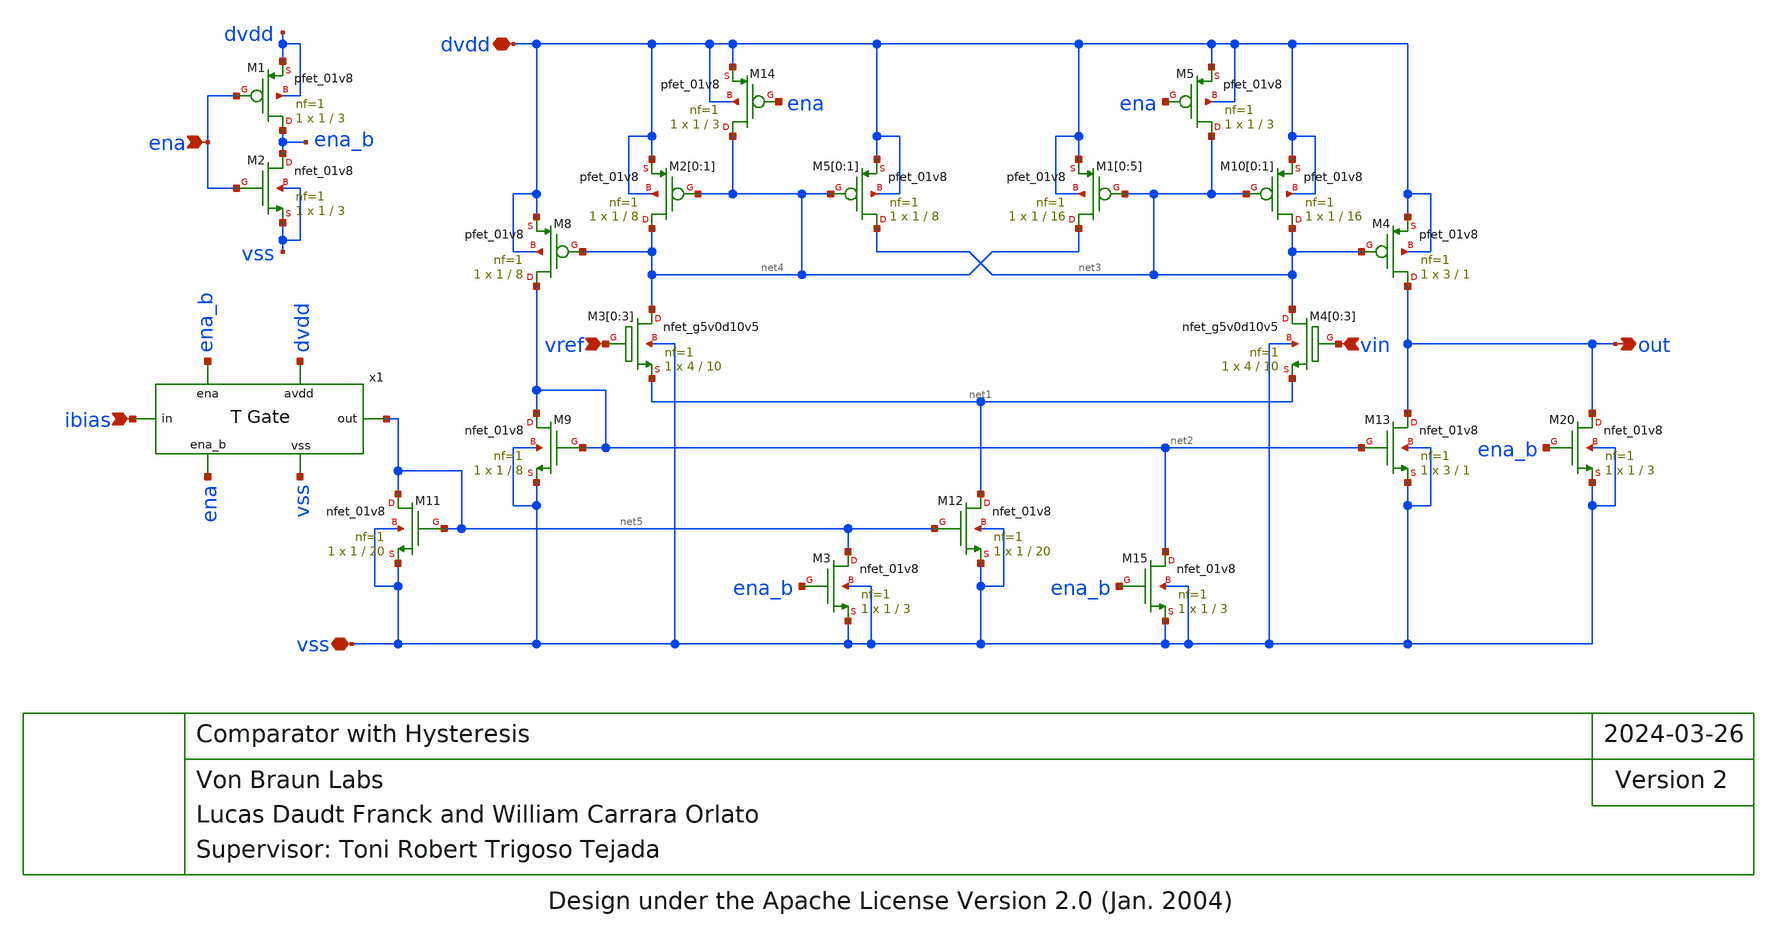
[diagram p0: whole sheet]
** sch_path: blocks/comp_hyst/xschem/comp_hyst.sch
* Design under the Apache License Version 2.0 (Jan. 2004)
**.subckt comp_hyst dvdd vref vin out ibias ena vss
*.iopin dvdd
*.ipin vref
*.ipin vin
*.opin out
*.ipin ibias
*.ipin ena
*.iopin vss
XM5[0] net3 net4 dvdd dvdd sky130_fd_pr__pfet_01v8 L=8 W=1 nf=1 ad='int((nf+1)/2) * W/nf * 0.29' as='int((nf+2)/2) * W/nf * 0.29'
+ pd='2*int((nf+1)/2) * (W/nf + 0.29)' ps='2*int((nf+2)/2) * (W/nf + 0.29)' nrd='0.29 / W' nrs='0.29 / W'
+ sa=0 sb=0 sd=0 mult=1 m=1
XM5[1] net3 net4 dvdd dvdd sky130_fd_pr__pfet_01v8 L=8 W=1 nf=1 ad='int((nf+1)/2) * W/nf * 0.29' as='int((nf+2)/2) * W/nf * 0.29'
+ pd='2*int((nf+1)/2) * (W/nf + 0.29)' ps='2*int((nf+2)/2) * (W/nf + 0.29)' nrd='0.29 / W' nrs='0.29 / W'
+ sa=0 sb=0 sd=0 mult=1 m=1
XM2[0] net4 net4 dvdd dvdd sky130_fd_pr__pfet_01v8 L=8 W=1 nf=1 ad='int((nf+1)/2) * W/nf * 0.29' as='int((nf+2)/2) * W/nf * 0.29'
+ pd='2*int((nf+1)/2) * (W/nf + 0.29)' ps='2*int((nf+2)/2) * (W/nf + 0.29)' nrd='0.29 / W' nrs='0.29 / W'
+ sa=0 sb=0 sd=0 mult=1 m=1
XM2[1] net4 net4 dvdd dvdd sky130_fd_pr__pfet_01v8 L=8 W=1 nf=1 ad='int((nf+1)/2) * W/nf * 0.29' as='int((nf+2)/2) * W/nf * 0.29'
+ pd='2*int((nf+1)/2) * (W/nf + 0.29)' ps='2*int((nf+2)/2) * (W/nf + 0.29)' nrd='0.29 / W' nrs='0.29 / W'
+ sa=0 sb=0 sd=0 mult=1 m=1
XM8 net2 net4 dvdd dvdd sky130_fd_pr__pfet_01v8 L=8 W=1 nf=1 ad='int((nf+1)/2) * W/nf * 0.29' as='int((nf+2)/2) * W/nf * 0.29'
+ pd='2*int((nf+1)/2) * (W/nf + 0.29)' ps='2*int((nf+2)/2) * (W/nf + 0.29)' nrd='0.29 / W' nrs='0.29 / W'
+ sa=0 sb=0 sd=0 mult=1 m=1
XM10[0] net3 net3 dvdd dvdd sky130_fd_pr__pfet_01v8 L=16 W=1 nf=1 ad='int((nf+1)/2) * W/nf * 0.29' as='int((nf+2)/2) * W/nf * 0.29'
+ pd='2*int((nf+1)/2) * (W/nf + 0.29)' ps='2*int((nf+2)/2) * (W/nf + 0.29)' nrd='0.29 / W' nrs='0.29 / W'
+ sa=0 sb=0 sd=0 mult=1 m=1
XM10[1] net3 net3 dvdd dvdd sky130_fd_pr__pfet_01v8 L=16 W=1 nf=1 ad='int((nf+1)/2) * W/nf * 0.29' as='int((nf+2)/2) * W/nf * 0.29'
+ pd='2*int((nf+1)/2) * (W/nf + 0.29)' ps='2*int((nf+2)/2) * (W/nf + 0.29)' nrd='0.29 / W' nrs='0.29 / W'
+ sa=0 sb=0 sd=0 mult=1 m=1
XM11 net5 net5 vss vss sky130_fd_pr__nfet_01v8 L=20 W=1 nf=1 ad='int((nf+1)/2) * W/nf * 0.29' as='int((nf+2)/2) * W/nf * 0.29'
+ pd='2*int((nf+1)/2) * (W/nf + 0.29)' ps='2*int((nf+2)/2) * (W/nf + 0.29)' nrd='0.29 / W' nrs='0.29 / W'
+ sa=0 sb=0 sd=0 mult=1 m=1
XM12 net1 net5 vss vss sky130_fd_pr__nfet_01v8 L=20 W=1 nf=1 ad='int((nf+1)/2) * W/nf * 0.29' as='int((nf+2)/2) * W/nf * 0.29'
+ pd='2*int((nf+1)/2) * (W/nf + 0.29)' ps='2*int((nf+2)/2) * (W/nf + 0.29)' nrd='0.29 / W' nrs='0.29 / W'
+ sa=0 sb=0 sd=0 mult=1 m=1
XM4 out net3 dvdd dvdd sky130_fd_pr__pfet_01v8 L=1 W=3 nf=1 ad='int((nf+1)/2) * W/nf * 0.29' as='int((nf+2)/2) * W/nf * 0.29'
+ pd='2*int((nf+1)/2) * (W/nf + 0.29)' ps='2*int((nf+2)/2) * (W/nf + 0.29)' nrd='0.29 / W' nrs='0.29 / W'
+ sa=0 sb=0 sd=0 mult=1 m=1
XM13 out net2 vss vss sky130_fd_pr__nfet_01v8 L=1 W=3 nf=1 ad='int((nf+1)/2) * W/nf * 0.29' as='int((nf+2)/2) * W/nf * 0.29'
+ pd='2*int((nf+1)/2) * (W/nf + 0.29)' ps='2*int((nf+2)/2) * (W/nf + 0.29)' nrd='0.29 / W' nrs='0.29 / W'
+ sa=0 sb=0 sd=0 mult=1 m=1
XM20 out ena_b vss vss sky130_fd_pr__nfet_01v8 L=3 W=1 nf=1 ad='int((nf+1)/2) * W/nf * 0.29' as='int((nf+2)/2) * W/nf * 0.29'
+ pd='2*int((nf+1)/2) * (W/nf + 0.29)' ps='2*int((nf+2)/2) * (W/nf + 0.29)' nrd='0.29 / W' nrs='0.29 / W'
+ sa=0 sb=0 sd=0 mult=1 m=1
XM3[0] net4 vref net1 vss sky130_fd_pr__nfet_g5v0d10v5 L=10 W=4 nf=1 ad='int((nf+1)/2) * W/nf * 0.29'
+ as='int((nf+2)/2) * W/nf * 0.29' pd='2*int((nf+1)/2) * (W/nf + 0.29)' ps='2*int((nf+2)/2) * (W/nf + 0.29)'
+ nrd='0.29 / W' nrs='0.29 / W' sa=0 sb=0 sd=0 mult=1 m=1
XM3[1] net4 vref net1 vss sky130_fd_pr__nfet_g5v0d10v5 L=10 W=4 nf=1 ad='int((nf+1)/2) * W/nf * 0.29'
+ as='int((nf+2)/2) * W/nf * 0.29' pd='2*int((nf+1)/2) * (W/nf + 0.29)' ps='2*int((nf+2)/2) * (W/nf + 0.29)'
+ nrd='0.29 / W' nrs='0.29 / W' sa=0 sb=0 sd=0 mult=1 m=1
XM3[2] net4 vref net1 vss sky130_fd_pr__nfet_g5v0d10v5 L=10 W=4 nf=1 ad='int((nf+1)/2) * W/nf * 0.29'
+ as='int((nf+2)/2) * W/nf * 0.29' pd='2*int((nf+1)/2) * (W/nf + 0.29)' ps='2*int((nf+2)/2) * (W/nf + 0.29)'
+ nrd='0.29 / W' nrs='0.29 / W' sa=0 sb=0 sd=0 mult=1 m=1
XM3[3] net4 vref net1 vss sky130_fd_pr__nfet_g5v0d10v5 L=10 W=4 nf=1 ad='int((nf+1)/2) * W/nf * 0.29'
+ as='int((nf+2)/2) * W/nf * 0.29' pd='2*int((nf+1)/2) * (W/nf + 0.29)' ps='2*int((nf+2)/2) * (W/nf + 0.29)'
+ nrd='0.29 / W' nrs='0.29 / W' sa=0 sb=0 sd=0 mult=1 m=1
XM4[0] net3 vin net1 vss sky130_fd_pr__nfet_g5v0d10v5 L=10 W=4 nf=1 ad='int((nf+1)/2) * W/nf * 0.29'
+ as='int((nf+2)/2) * W/nf * 0.29' pd='2*int((nf+1)/2) * (W/nf + 0.29)' ps='2*int((nf+2)/2) * (W/nf + 0.29)'
+ nrd='0.29 / W' nrs='0.29 / W' sa=0 sb=0 sd=0 mult=1 m=1
XM4[1] net3 vin net1 vss sky130_fd_pr__nfet_g5v0d10v5 L=10 W=4 nf=1 ad='int((nf+1)/2) * W/nf * 0.29'
+ as='int((nf+2)/2) * W/nf * 0.29' pd='2*int((nf+1)/2) * (W/nf + 0.29)' ps='2*int((nf+2)/2) * (W/nf + 0.29)'
+ nrd='0.29 / W' nrs='0.29 / W' sa=0 sb=0 sd=0 mult=1 m=1
XM4[2] net3 vin net1 vss sky130_fd_pr__nfet_g5v0d10v5 L=10 W=4 nf=1 ad='int((nf+1)/2) * W/nf * 0.29'
+ as='int((nf+2)/2) * W/nf * 0.29' pd='2*int((nf+1)/2) * (W/nf + 0.29)' ps='2*int((nf+2)/2) * (W/nf + 0.29)'
+ nrd='0.29 / W' nrs='0.29 / W' sa=0 sb=0 sd=0 mult=1 m=1
XM4[3] net3 vin net1 vss sky130_fd_pr__nfet_g5v0d10v5 L=10 W=4 nf=1 ad='int((nf+1)/2) * W/nf * 0.29'
+ as='int((nf+2)/2) * W/nf * 0.29' pd='2*int((nf+1)/2) * (W/nf + 0.29)' ps='2*int((nf+2)/2) * (W/nf + 0.29)'
+ nrd='0.29 / W' nrs='0.29 / W' sa=0 sb=0 sd=0 mult=1 m=1
XM3 net5 ena_b vss vss sky130_fd_pr__nfet_01v8 L=3 W=1 nf=1 ad='int((nf+1)/2) * W/nf * 0.29' as='int((nf+2)/2) * W/nf * 0.29'
+ pd='2*int((nf+1)/2) * (W/nf + 0.29)' ps='2*int((nf+2)/2) * (W/nf + 0.29)' nrd='0.29 / W' nrs='0.29 / W'
+ sa=0 sb=0 sd=0 mult=1 m=1
XM1[0] net4 net3 dvdd dvdd sky130_fd_pr__pfet_01v8 L=16 W=1 nf=1 ad='int((nf+1)/2) * W/nf * 0.29' as='int((nf+2)/2) * W/nf * 0.29'
+ pd='2*int((nf+1)/2) * (W/nf + 0.29)' ps='2*int((nf+2)/2) * (W/nf + 0.29)' nrd='0.29 / W' nrs='0.29 / W'
+ sa=0 sb=0 sd=0 mult=1 m=1
XM1[1] net4 net3 dvdd dvdd sky130_fd_pr__pfet_01v8 L=16 W=1 nf=1 ad='int((nf+1)/2) * W/nf * 0.29' as='int((nf+2)/2) * W/nf * 0.29'
+ pd='2*int((nf+1)/2) * (W/nf + 0.29)' ps='2*int((nf+2)/2) * (W/nf + 0.29)' nrd='0.29 / W' nrs='0.29 / W'
+ sa=0 sb=0 sd=0 mult=1 m=1
XM1[2] net4 net3 dvdd dvdd sky130_fd_pr__pfet_01v8 L=16 W=1 nf=1 ad='int((nf+1)/2) * W/nf * 0.29' as='int((nf+2)/2) * W/nf * 0.29'
+ pd='2*int((nf+1)/2) * (W/nf + 0.29)' ps='2*int((nf+2)/2) * (W/nf + 0.29)' nrd='0.29 / W' nrs='0.29 / W'
+ sa=0 sb=0 sd=0 mult=1 m=1
XM1[3] net4 net3 dvdd dvdd sky130_fd_pr__pfet_01v8 L=16 W=1 nf=1 ad='int((nf+1)/2) * W/nf * 0.29' as='int((nf+2)/2) * W/nf * 0.29'
+ pd='2*int((nf+1)/2) * (W/nf + 0.29)' ps='2*int((nf+2)/2) * (W/nf + 0.29)' nrd='0.29 / W' nrs='0.29 / W'
+ sa=0 sb=0 sd=0 mult=1 m=1
XM1[4] net4 net3 dvdd dvdd sky130_fd_pr__pfet_01v8 L=16 W=1 nf=1 ad='int((nf+1)/2) * W/nf * 0.29' as='int((nf+2)/2) * W/nf * 0.29'
+ pd='2*int((nf+1)/2) * (W/nf + 0.29)' ps='2*int((nf+2)/2) * (W/nf + 0.29)' nrd='0.29 / W' nrs='0.29 / W'
+ sa=0 sb=0 sd=0 mult=1 m=1
XM1[5] net4 net3 dvdd dvdd sky130_fd_pr__pfet_01v8 L=16 W=1 nf=1 ad='int((nf+1)/2) * W/nf * 0.29' as='int((nf+2)/2) * W/nf * 0.29'
+ pd='2*int((nf+1)/2) * (W/nf + 0.29)' ps='2*int((nf+2)/2) * (W/nf + 0.29)' nrd='0.29 / W' nrs='0.29 / W'
+ sa=0 sb=0 sd=0 mult=1 m=1
XM9 net2 net2 vss vss sky130_fd_pr__nfet_01v8 L=8 W=1 nf=1 ad='int((nf+1)/2) * W/nf * 0.29' as='int((nf+2)/2) * W/nf * 0.29'
+ pd='2*int((nf+1)/2) * (W/nf + 0.29)' ps='2*int((nf+2)/2) * (W/nf + 0.29)' nrd='0.29 / W' nrs='0.29 / W'
+ sa=0 sb=0 sd=0 mult=1 m=1
XM5 net3 ena dvdd dvdd sky130_fd_pr__pfet_01v8 L=3 W=1 nf=1 ad='int((nf+1)/2) * W/nf * 0.29' as='int((nf+2)/2) * W/nf * 0.29'
+ pd='2*int((nf+1)/2) * (W/nf + 0.29)' ps='2*int((nf+2)/2) * (W/nf + 0.29)' nrd='0.29 / W' nrs='0.29 / W'
+ sa=0 sb=0 sd=0 mult=1 m=1
XM14 net4 ena dvdd dvdd sky130_fd_pr__pfet_01v8 L=3 W=1 nf=1 ad='int((nf+1)/2) * W/nf * 0.29' as='int((nf+2)/2) * W/nf * 0.29'
+ pd='2*int((nf+1)/2) * (W/nf + 0.29)' ps='2*int((nf+2)/2) * (W/nf + 0.29)' nrd='0.29 / W' nrs='0.29 / W'
+ sa=0 sb=0 sd=0 mult=1 m=1
XM15 net2 ena_b vss vss sky130_fd_pr__nfet_01v8 L=3 W=1 nf=1 ad='int((nf+1)/2) * W/nf * 0.29' as='int((nf+2)/2) * W/nf * 0.29'
+ pd='2*int((nf+1)/2) * (W/nf + 0.29)' ps='2*int((nf+2)/2) * (W/nf + 0.29)' nrd='0.29 / W' nrs='0.29 / W'
+ sa=0 sb=0 sd=0 mult=1 m=1
XM1 ena_b ena dvdd dvdd sky130_fd_pr__pfet_01v8 L=3 W=1 nf=1 ad='int((nf+1)/2) * W/nf * 0.29' as='int((nf+2)/2) * W/nf * 0.29'
+ pd='2*int((nf+1)/2) * (W/nf + 0.29)' ps='2*int((nf+2)/2) * (W/nf + 0.29)' nrd='0.29 / W' nrs='0.29 / W'
+ sa=0 sb=0 sd=0 mult=1 m=1
XM2 ena_b ena vss vss sky130_fd_pr__nfet_01v8 L=3 W=1 nf=1 ad='int((nf+1)/2) * W/nf * 0.29' as='int((nf+2)/2) * W/nf * 0.29'
+ pd='2*int((nf+1)/2) * (W/nf + 0.29)' ps='2*int((nf+2)/2) * (W/nf + 0.29)' nrd='0.29 / W' nrs='0.29 / W'
+ sa=0 sb=0 sd=0 mult=1 m=1
x1 ibias ena ena_b dvdd vss net5 trans_gate
**.ends

* expanding   symbol:  trans_gate.sym # of pins=6
** sym_path: blocks/comp_hyst/xschem/trans_gate.sym
** sch_path: blocks/comp_hyst/xschem/trans_gate.sch
.subckt trans_gate in ena_b ena avdd vss out
*.iopin avdd
*.iopin vss
*.ipin ena
*.ipin ena_b
*.ipin in
*.ipin out
XM1 in ena_b out vss sky130_fd_pr__nfet_g5v0d10v5 L=5 W=1 nf=1 ad='int((nf+1)/2) * W/nf * 0.29' as='int((nf+2)/2) * W/nf * 0.29'
+ pd='2*int((nf+1)/2) * (W/nf + 0.29)' ps='2*int((nf+2)/2) * (W/nf + 0.29)' nrd='0.29 / W' nrs='0.29 / W'
+ sa=0 sb=0 sd=0 mult=1 m=1
XM2 in ena out avdd sky130_fd_pr__pfet_g5v0d10v5 L=5 W=6 nf=1 ad='int((nf+1)/2) * W/nf * 0.29' as='int((nf+2)/2) * W/nf * 0.29'
+ pd='2*int((nf+1)/2) * (W/nf + 0.29)' ps='2*int((nf+2)/2) * (W/nf + 0.29)' nrd='0.29 / W' nrs='0.29 / W'
+ sa=0 sb=0 sd=0 mult=1 m=1
.ends

.end
